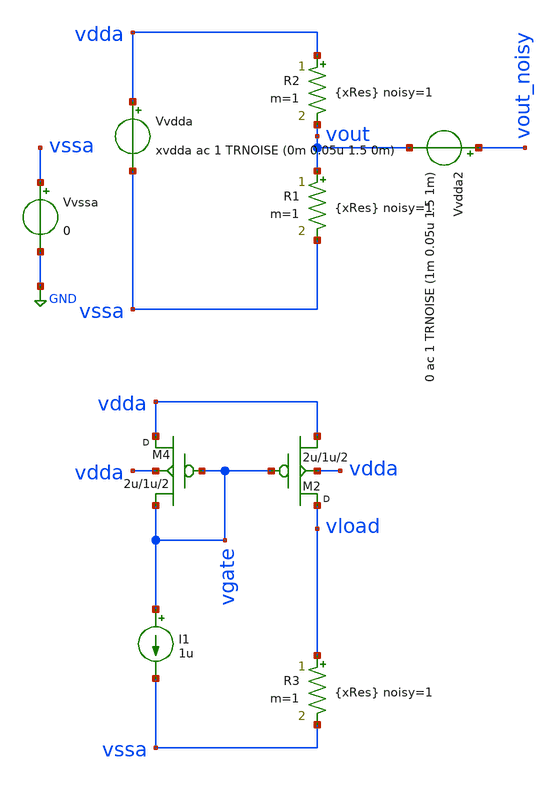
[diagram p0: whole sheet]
** sch_path: Running_AC_noise_summary_in_ngspice/tran_noise.sch
**.subckt tran_noise
Vvssa vssa GND 0
Vvdda vdda vssa xvdda ac 1 TRNOISE (0m 0.05u 1.5 0m)
R1 vout vssa {xRes} noisy=1 m=1
R2 vdda vout {xRes} noisy=1 m=1
M2 vload vgate vdda vdda pmosx w=2u l=1u m=2
M4 vdda vgate vgate vdda pmosx w=2u l=1u m=2
I1 vgate vssa 1u
R3 vload vssa {xRes} noisy=1 m=1
Vvdda2 vout_noisy vout 0 ac 1 TRNOISE (1m 0.05u 1.5 1m)
**** begin user architecture code

* default BSIM models
.model nmosx nmos level=54 version=4.8.2
.model pmosx pmos level=54 version=4.8.2

* parameter definition
.param xvdda = 1
.param xRes = 1k

.control

destroy all
save all

* 1. Transient Analysis:
let xtsim = 5u;

   tran 1n $&xtsim
   remzerovec
   write tran_noise_tran1.raw

* 2. Noise Analysis:


let xfmax = 100G;

* Perform noise analysis on resistor divider
noise v(vout) Vvdda dec 10 1 $&xfmax 1

* Perform noise analysis on current mirror into resistor load
*noise v(vload) Vvdda dec 10 1 $&xfmax 1

* plot total integrted noise up to xfmax
print v(onoise_total)

* save integrated noise data
remzerovec
write tran_noise_integrated.raw

* save noise density data
setplot noise1
remzerovec
write tran_noise_density.raw

* ngspice plots (optional)
* plot noise density
* plot onoise_spectrum

* calculate total integrated noise to see if it matches v(onoise_total)
* this is only plotted in ngspice as shown on line 55
let vnoise_op_int = sqrt(integ(onoise_spectrum*onoise_spectrum))
*echo $&vnoise_op_int

* ngspice plots (optional)
* plot integrated noise
* plot vnoise_op_int xlog

* save integrated noise data in ascii format for awk script post-processing
* !Important: Set back to integrated noise data contained in noise2!
setplot noise2
set filetype=ascii
remzerovec
write tran_noise_integrated_ascii.raw

setplot
.endc



**** end user architecture code
**.ends
.GLOBAL GND
.end
